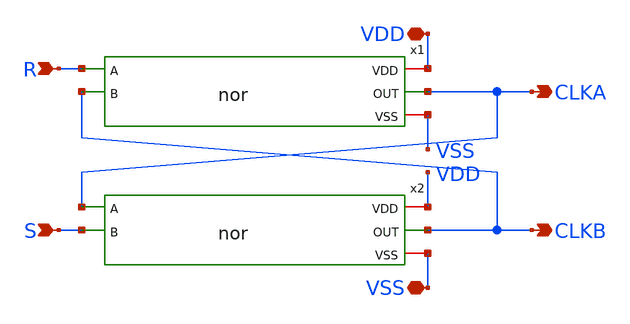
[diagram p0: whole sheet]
** sch_path: designs/relaxation-oscillator/sr-latch.sch
**.subckt sr-latch VDD VSS CLKA CLKB R S
*.iopin VDD
*.iopin VSS
*.opin CLKA
*.opin CLKB
*.ipin R
*.ipin S
x1 VDD R CLKB CLKA VSS nor
x2 VDD CLKA S CLKB VSS nor
**.ends

* expanding   symbol:  nor.sym # of pins=5
** sym_path: designs/relaxation-oscillator/nor.sym
** sch_path: designs/relaxation-oscillator/nor.sch
.subckt nor VDD A B OUT VSS
*.ipin A
*.ipin B
*.iopin VDD
*.iopin VSS
*.opin OUT
XM1 net1 A VDD VDD pfet_05v0 L=0.50u W=0.9u nf=1 ad='int((nf+1)/2) * W/nf * 0.18u' as='int((nf+2)/2) * W/nf * 0.18u'
+ pd='2*int((nf+1)/2) * (W/nf + 0.18u)' ps='2*int((nf+2)/2) * (W/nf + 0.18u)' nrd='0.18u / W' nrs='0.18u / W'
+ sa=0 sb=0 sd=0 m=1
XM2 OUT B net1 VDD pfet_05v0 L=0.50u W=0.9u nf=1 ad='int((nf+1)/2) * W/nf * 0.18u' as='int((nf+2)/2) * W/nf * 0.18u'
+ pd='2*int((nf+1)/2) * (W/nf + 0.18u)' ps='2*int((nf+2)/2) * (W/nf + 0.18u)' nrd='0.18u / W' nrs='0.18u / W'
+ sa=0 sb=0 sd=0 m=1
XM3 OUT A VSS VSS nfet_05v0 L=0.60u W=0.30u nf=1 ad='int((nf+1)/2) * W/nf * 0.18u' as='int((nf+2)/2) * W/nf * 0.18u'
+ pd='2*int((nf+1)/2) * (W/nf + 0.18u)' ps='2*int((nf+2)/2) * (W/nf + 0.18u)' nrd='0.18u / W' nrs='0.18u / W'
+ sa=0 sb=0 sd=0 m=1
XM4 OUT B VSS VSS nfet_05v0 L=0.60u W=0.30u nf=1 ad='int((nf+1)/2) * W/nf * 0.18u' as='int((nf+2)/2) * W/nf * 0.18u'
+ pd='2*int((nf+1)/2) * (W/nf + 0.18u)' ps='2*int((nf+2)/2) * (W/nf + 0.18u)' nrd='0.18u / W' nrs='0.18u / W'
+ sa=0 sb=0 sd=0 m=1
.ends

.end
